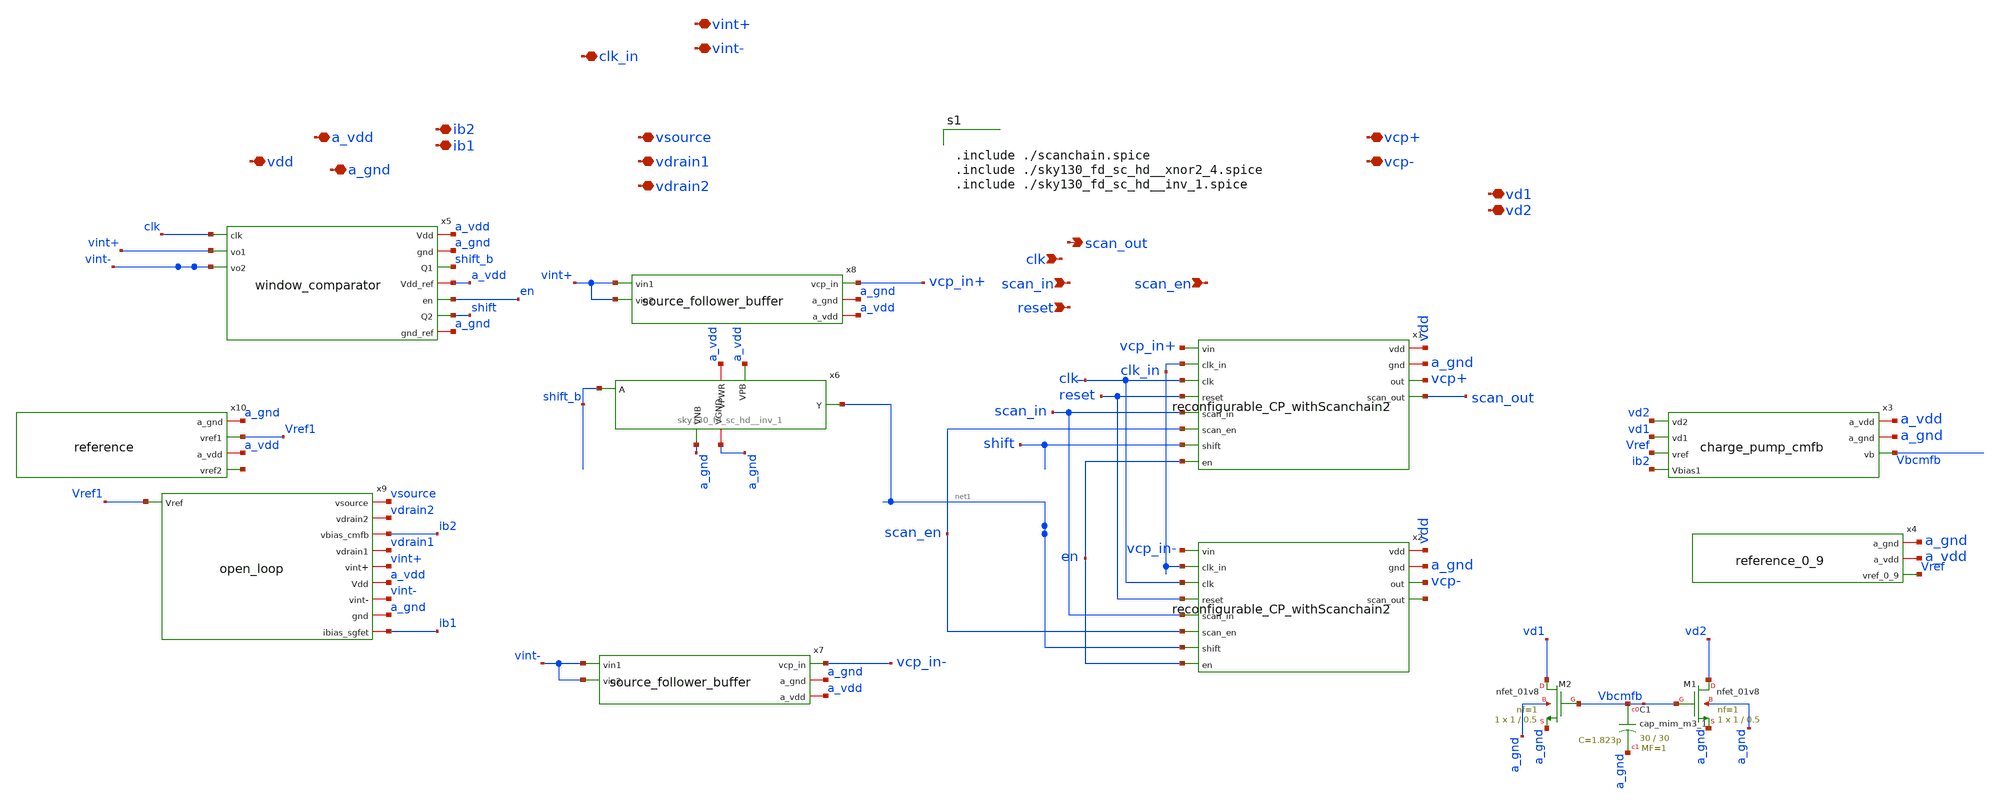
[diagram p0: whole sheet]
** sch_path: xschem/charge_pumps2/toplevel_schematic.sch
**.subckt toplevel_schematic clk_in vint+ vint- vsource vdrain1 vdrain2 ib2 ib1 a_gnd a_vdd vdd vcp+
*+ vcp- vd1 vd2 scan_out clk scan_in reset scan_en
*.iopin clk_in
*.iopin vint+
*.iopin vint-
*.iopin vsource
*.iopin vdrain1
*.iopin vdrain2
*.iopin ib2
*.iopin ib1
*.iopin a_gnd
*.iopin a_vdd
*.iopin vdd
*.iopin vcp+
*.iopin vcp-
*.iopin vd1
*.iopin vd2
*.opin scan_out
*.ipin clk
*.ipin scan_in
*.ipin reset
*.ipin scan_en
x1 vdd vcp_in+ a_gnd clk_in clk reset scan_in scan_en vcp+ shift en scan_out
+ reconfigurable_CP_withScanchain2
x2 vdd vcp_in- a_gnd clk_in clk reset scan_in scan_en vcp- net1 en net2
+ reconfigurable_CP_withScanchain2
XC1 Vbcmfb a_gnd sky130_fd_pr__cap_mim_m3_1 W=30 L=30 MF=1 m=1
x3 vd2 vd1 Vref ib2 a_vdd a_gnd Vbcmfb charge_pump_cmfb
x4 a_gnd a_vdd Vref reference_0_9
XM1 vd2 Vbcmfb a_gnd a_gnd sky130_fd_pr__nfet_01v8 L=0.5 W=1 nf=1 ad='int((nf+1)/2) * W/nf * 0.29' as='int((nf+2)/2) * W/nf * 0.29'
+ pd='2*int((nf+1)/2) * (W/nf + 0.29)' ps='2*int((nf+2)/2) * (W/nf + 0.29)' nrd='0.29 / W' nrs='0.29 / W'
+ sa=0 sb=0 sd=0 mult=1 m=1
XM2 vd1 Vbcmfb a_gnd a_gnd sky130_fd_pr__nfet_01v8 L=0.5 W=1 nf=1 ad='int((nf+1)/2) * W/nf * 0.29' as='int((nf+2)/2) * W/nf * 0.29'
+ pd='2*int((nf+1)/2) * (W/nf + 0.29)' ps='2*int((nf+2)/2) * (W/nf + 0.29)' nrd='0.29 / W' nrs='0.29 / W'
+ sa=0 sb=0 sd=0 mult=1 m=1
x5 a_vdd a_gnd clk vint+ shift_b vint- a_vdd en shift a_gnd window_comparator
x6 shift_b a_gnd a_gnd a_vdd a_vdd net1 sky130_fd_sc_hd__inv_1
x7 vcp_in- a_gnd vint- a_vdd vint- source_follower_buffer
x8 vcp_in+ a_gnd vint+ a_vdd vint+ source_follower_buffer
x9 vsource vdrain2 ib2 vdrain1 Vref1 vint+ a_vdd vint- a_gnd ib1 open_loop
x10 a_gnd Vref1 a_vdd net3 reference
**** begin user architecture code


.include ./scanchain.spice
.include ./sky130_fd_sc_hd__xnor2_4.spice
.include ./sky130_fd_sc_hd__inv_1.spice



** opencircuitdesign pdks install
.lib $::SKYWATER_MODELS/sky130.lib.spice tt


**** end user architecture code
**.ends
.end
